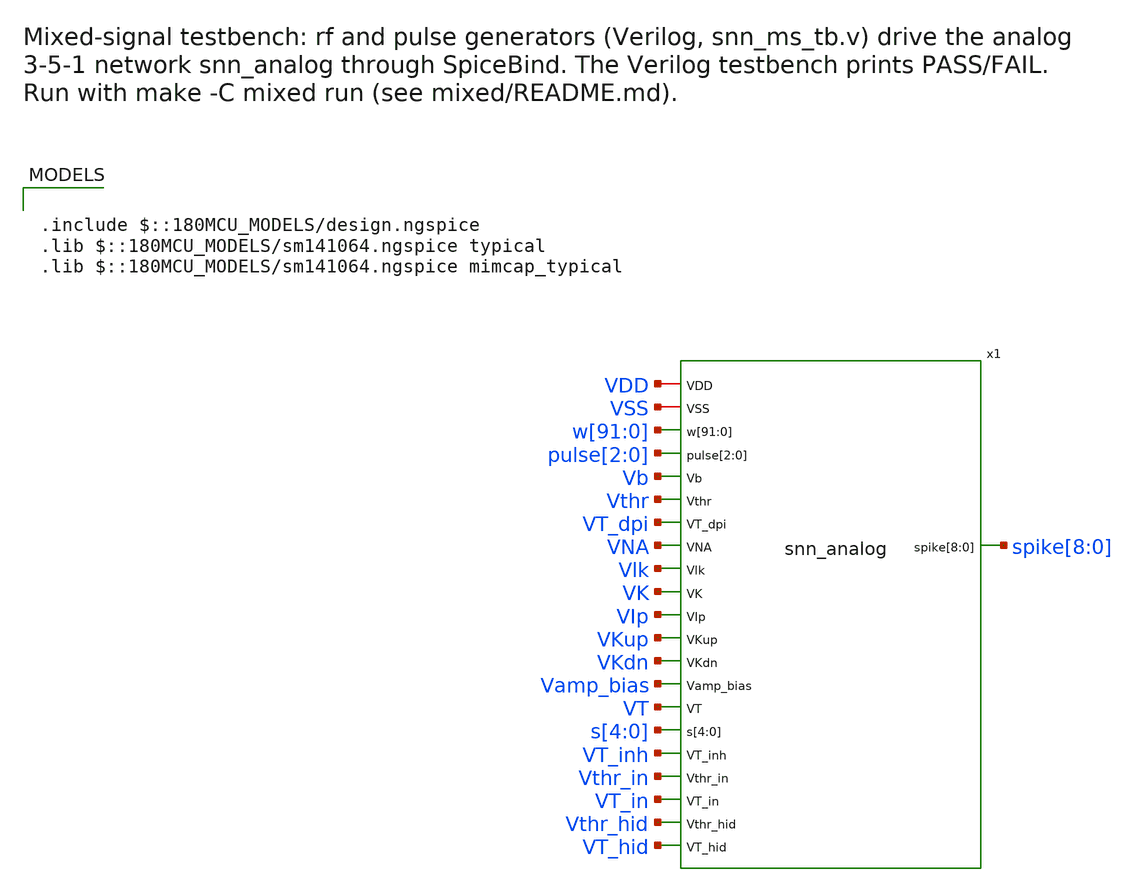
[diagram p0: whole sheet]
** sch_path: mixed/snn_ms_tb.sch
**.subckt snn_ms_tb
x1 VDD VSS w[91] w[90] w[89] w[88] w[87] w[86] w[85] w[84] w[83] w[82] w[81] w[80] w[79] w[78] w[77]
+ w[76] w[75] w[74] w[73] w[72] w[71] w[70] w[69] w[68] w[67] w[66] w[65] w[64] w[63] w[62] w[61] w[60]
+ w[59] w[58] w[57] w[56] w[55] w[54] w[53] w[52] w[51] w[50] w[49] w[48] w[47] w[46] w[45] w[44] w[43]
+ w[42] w[41] w[40] w[39] w[38] w[37] w[36] w[35] w[34] w[33] w[32] w[31] w[30] w[29] w[28] w[27] w[26]
+ w[25] w[24] w[23] w[22] w[21] w[20] w[19] w[18] w[17] w[16] w[15] w[14] w[13] w[12] w[11] w[10] w[9] w[8]
+ w[7] w[6] w[5] w[4] w[3] w[2] w[1] w[0] pulse[2] pulse[1] pulse[0] Vb Vthr VT_dpi VNA Vlk VK VIp VKup
+ VKdn Vamp_bias VT s[4] s[3] s[2] s[1] s[0] VT_inh Vthr_in VT_in Vthr_hid VT_hid spike[8] spike[7]
+ spike[6] spike[5] spike[4] spike[3] spike[2] spike[1] spike[0] snn_analog
**** begin user architecture code

.include $::180MCU_MODELS/design.ngspice
.lib $::180MCU_MODELS/sm141064.ngspice typical
.lib $::180MCU_MODELS/sm141064.ngspice mimcap_typical



* Nets driven from Verilog: SpiceBind sets these external sources (snn_ms_tb.v).
Vw[0] w[0] 0 0 external
Vw[1] w[1] 0 0 external
Vw[2] w[2] 0 0 external
Vw[3] w[3] 0 0 external
Vw[4] w[4] 0 0 external
Vw[5] w[5] 0 0 external
Vw[6] w[6] 0 0 external
Vw[7] w[7] 0 0 external
Vw[8] w[8] 0 0 external
Vw[9] w[9] 0 0 external
Vw[10] w[10] 0 0 external
Vw[11] w[11] 0 0 external
Vw[12] w[12] 0 0 external
Vw[13] w[13] 0 0 external
Vw[14] w[14] 0 0 external
Vw[15] w[15] 0 0 external
Vw[16] w[16] 0 0 external
Vw[17] w[17] 0 0 external
Vw[18] w[18] 0 0 external
Vw[19] w[19] 0 0 external
Vw[20] w[20] 0 0 external
Vw[21] w[21] 0 0 external
Vw[22] w[22] 0 0 external
Vw[23] w[23] 0 0 external
Vw[24] w[24] 0 0 external
Vw[25] w[25] 0 0 external
Vw[26] w[26] 0 0 external
Vw[27] w[27] 0 0 external
Vw[28] w[28] 0 0 external
Vw[29] w[29] 0 0 external
Vw[30] w[30] 0 0 external
Vw[31] w[31] 0 0 external
Vw[32] w[32] 0 0 external
Vw[33] w[33] 0 0 external
Vw[34] w[34] 0 0 external
Vw[35] w[35] 0 0 external
Vw[36] w[36] 0 0 external
Vw[37] w[37] 0 0 external
Vw[38] w[38] 0 0 external
Vw[39] w[39] 0 0 external
Vw[40] w[40] 0 0 external
Vw[41] w[41] 0 0 external
Vw[42] w[42] 0 0 external
Vw[43] w[43] 0 0 external
Vw[44] w[44] 0 0 external
Vw[45] w[45] 0 0 external
Vw[46] w[46] 0 0 external
Vw[47] w[47] 0 0 external
Vw[48] w[48] 0 0 external
Vw[49] w[49] 0 0 external
Vw[50] w[50] 0 0 external
Vw[51] w[51] 0 0 external
Vw[52] w[52] 0 0 external
Vw[53] w[53] 0 0 external
Vw[54] w[54] 0 0 external
Vw[55] w[55] 0 0 external
Vw[56] w[56] 0 0 external
Vw[57] w[57] 0 0 external
Vw[58] w[58] 0 0 external
Vw[59] w[59] 0 0 external
Vw[60] w[60] 0 0 external
Vw[61] w[61] 0 0 external
Vw[62] w[62] 0 0 external
Vw[63] w[63] 0 0 external
Vw[64] w[64] 0 0 external
Vw[65] w[65] 0 0 external
Vw[66] w[66] 0 0 external
Vw[67] w[67] 0 0 external
Vw[68] w[68] 0 0 external
Vw[69] w[69] 0 0 external
Vw[70] w[70] 0 0 external
Vw[71] w[71] 0 0 external
Vw[72] w[72] 0 0 external
Vw[73] w[73] 0 0 external
Vw[74] w[74] 0 0 external
Vw[75] w[75] 0 0 external
Vw[76] w[76] 0 0 external
Vw[77] w[77] 0 0 external
Vw[78] w[78] 0 0 external
Vw[79] w[79] 0 0 external
Vw[80] w[80] 0 0 external
Vw[81] w[81] 0 0 external
Vw[82] w[82] 0 0 external
Vw[83] w[83] 0 0 external
Vw[84] w[84] 0 0 external
Vw[85] w[85] 0 0 external
Vw[86] w[86] 0 0 external
Vw[87] w[87] 0 0 external
Vw[88] w[88] 0 0 external
Vw[89] w[89] 0 0 external
Vw[90] w[90] 0 0 external
Vw[91] w[91] 0 0 external
Vpulse[0] pulse[0] 0 0 external
Vpulse[1] pulse[1] 0 0 external
Vpulse[2] pulse[2] 0 0 external




* Supplies and biases, as in analog/neuron/DACs-DPI-neuron.sch
* Parameter names start with p_: a .param with the same name as a net made ngspice
* rename that net to {name} on the long x1 line, leaving the biases unconnected.
* DPIs are DPI_sized (W 0.88u, L 1.12u); biases per layer from the Monte Carlo runs in
* analog/testbenches/xor (README.md): output keeps the old gain and tau, input relays fire one
* spike per pulse, hidden layer in threshold mode, Vlk 0.48
.param p_vdd=3.3 p_vtau=0.5096 p_iref=14.42n
.param p_vthr=2.7703
.param p_vthr_in=2.4 p_vtau_in=0.72 p_vthr_hid=2.5 p_vtau_hid=0.6225
.param p_vlk=0.48 p_vamp_bias=0.535 p_vip=0.573 p_vna=1.93 p_vkup=2.35 p_vk=1.22 p_vkdn=0.588
+ p_vt=1.66
Vdd VDD 0 {p_vdd}
Vss VSS 0 0
* DAC unit current: Iref into a diode-connected unit current source (w[0] = 15 nA)
Iref VDD Vb {p_iref}
XMref Vb Vb 0 0 nfet_03v3 L=8u W=1u nf=1
Vthr Vthr 0 {p_vthr}
Vtau VDD VT_dpi {p_vtau}
* Output inhibitory synapse (DPI_inh): same tau. The scenarios use no inhibition, so the
* sign bits s[4:0] of the hidden -> output synapses are 0 (not driven from Verilog yet).
Vtau_i VDD VT_inh {p_vtau}
Vthr_in Vthr_in 0 {p_vthr_in}
Vtau_in VDD VT_in {p_vtau_in}
Vthr_hid Vthr_hid 0 {p_vthr_hid}
Vtau_hid VDD VT_hid {p_vtau_hid}
Vs0 s[0] 0 0
Vs1 s[1] 0 0
Vs2 s[2] 0 0
Vs3 s[3] 0 0
Vs4 s[4] 0 0
Vlk Vlk VSS {p_vlk}
VK VK VSS {p_vk}
VNA VNA VSS {p_vna}
VKup VKup VSS {p_vkup}
VKdn VKdn VSS {p_vkdn}
VIp VIp VSS {p_vip}
VT VT VSS {p_vt}
Vamp_bias Vamp_bias VSS {p_vamp_bias}




* Start every membrane and spike output at 0 V: without this the DC operating point of the
* sized network does not converge (gmin and source stepping both fail) and the run hangs
.ic v(x1.VMEM_0)=0 v(x1.VMEM_1)=0 v(x1.VMEM_2)=0 v(x1.VMEM_3)=0 v(x1.VMEM_4)=0 v(x1.VMEM_5)=0
+ v(x1.VMEM_6)=0 v(x1.VMEM_7)=0 v(x1.VMEM_8)=0 v(spike[0])=0 v(spike[1])=0 v(spike[2])=0 v(spike[3])=0 v(spike[4])=0
+ v(spike[5])=0 v(spike[6])=0 v(spike[7])=0 v(spike[8])=0
* Gear integration: trap makes the DPI output current ring after each reset (entry 46)
.options method=gear
.save v(spike[0]) v(spike[1]) v(spike[2]) v(spike[3]) v(spike[4]) v(spike[5]) v(spike[6]) v(spike[7]) v(spike[8]) v(pulse[0]) v(pulse[1]) v(pulse[2]) v(scen[0]) v(scen[1]) v(scen[2]) v(running) v(done) v(x1.VMEM_0) v(x1.VMEM_1) v(x1.VMEM_2) v(x1.VMEM_3) v(x1.VMEM_4) v(x1.VMEM_5) v(x1.VMEM_6) v(x1.VMEM_7) v(x1.VMEM_8)
* Runs until the Verilog testbench calls $finish. ngspice reserves memory for tstop/step
* points, so a huge bound crashes it (1 s did): keep this just above the longest run.
.tran 0.1u 100m 0 0.1u


**** end user architecture code
**.ends
.end
